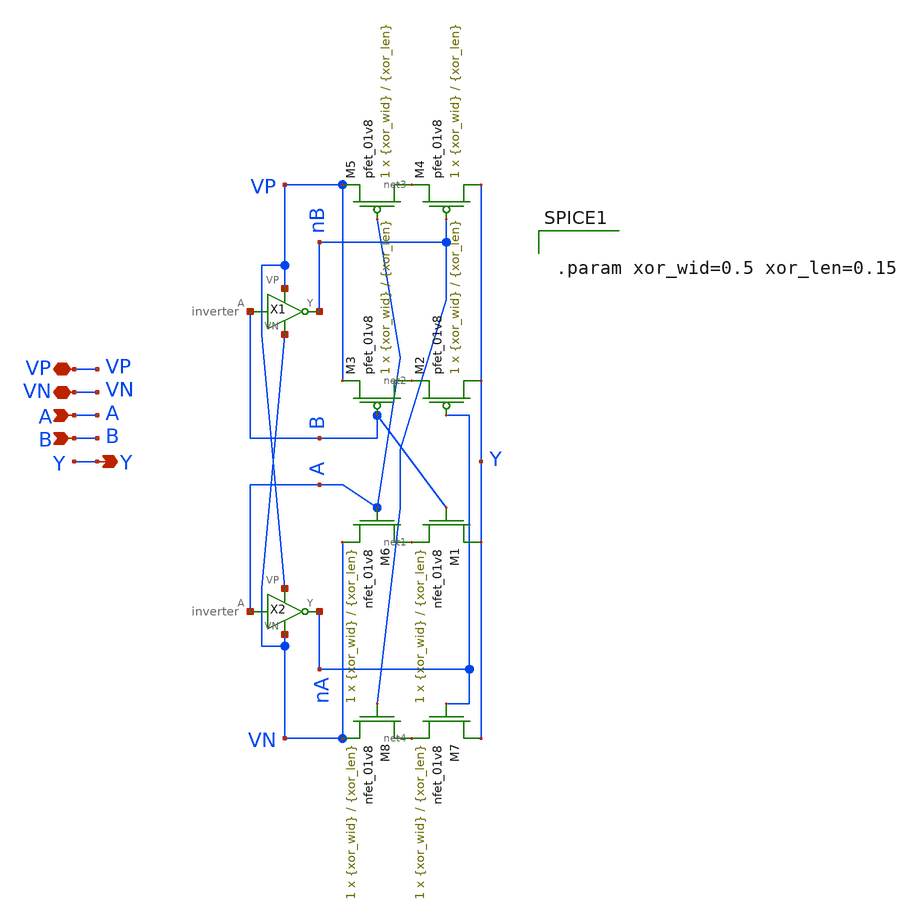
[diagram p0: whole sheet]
** sch_path: LDS/LDS_xor.sch
**.subckt LDS_xor VN VP Y A B
*.iopin VN
*.iopin VP
*.opin Y
*.ipin A
*.ipin B
X2 A nA VP VN inverter
X1 B nB VP VN inverter
XM1 Y B net1 VN sky130_fd_pr__nfet_01v8 L={xor_len} W={xor_wid} nf=1 ad='int((nf+1)/2) * W/nf * 0.29'
+ as='int((nf+2)/2) * W/nf * 0.29' pd='2*int((nf+1)/2) * (W/nf + 0.29)' ps='2*int((nf+2)/2) * (W/nf + 0.29)'
+ nrd='0.29 / W' nrs='0.29 / W' sa=0 sb=0 sd=0 mult=1 m=1
XM2 Y nA net2 VP sky130_fd_pr__pfet_01v8 L={xor_len} W={xor_wid} nf=1 ad='int((nf+1)/2) * W/nf * 0.29'
+ as='int((nf+2)/2) * W/nf * 0.29' pd='2*int((nf+1)/2) * (W/nf + 0.29)' ps='2*int((nf+2)/2) * (W/nf + 0.29)'
+ nrd='0.29 / W' nrs='0.29 / W' sa=0 sb=0 sd=0 mult=1 m=1
XM3 net2 B VP VP sky130_fd_pr__pfet_01v8 L={xor_len} W={xor_wid} nf=1 ad='int((nf+1)/2) * W/nf * 0.29'
+ as='int((nf+2)/2) * W/nf * 0.29' pd='2*int((nf+1)/2) * (W/nf + 0.29)' ps='2*int((nf+2)/2) * (W/nf + 0.29)'
+ nrd='0.29 / W' nrs='0.29 / W' sa=0 sb=0 sd=0 mult=1 m=1
XM4 Y nB net3 VP sky130_fd_pr__pfet_01v8 L={xor_len} W={xor_wid} nf=1 ad='int((nf+1)/2) * W/nf * 0.29'
+ as='int((nf+2)/2) * W/nf * 0.29' pd='2*int((nf+1)/2) * (W/nf + 0.29)' ps='2*int((nf+2)/2) * (W/nf + 0.29)'
+ nrd='0.29 / W' nrs='0.29 / W' sa=0 sb=0 sd=0 mult=1 m=1
XM5 net3 A VP VP sky130_fd_pr__pfet_01v8 L={xor_len} W={xor_wid} nf=1 ad='int((nf+1)/2) * W/nf * 0.29'
+ as='int((nf+2)/2) * W/nf * 0.29' pd='2*int((nf+1)/2) * (W/nf + 0.29)' ps='2*int((nf+2)/2) * (W/nf + 0.29)'
+ nrd='0.29 / W' nrs='0.29 / W' sa=0 sb=0 sd=0 mult=1 m=1
XM6 net1 A VN VN sky130_fd_pr__nfet_01v8 L={xor_len} W={xor_wid} nf=1 ad='int((nf+1)/2) * W/nf * 0.29'
+ as='int((nf+2)/2) * W/nf * 0.29' pd='2*int((nf+1)/2) * (W/nf + 0.29)' ps='2*int((nf+2)/2) * (W/nf + 0.29)'
+ nrd='0.29 / W' nrs='0.29 / W' sa=0 sb=0 sd=0 mult=1 m=1
XM7 Y nA net4 VN sky130_fd_pr__nfet_01v8 L={xor_len} W={xor_wid} nf=1 ad='int((nf+1)/2) * W/nf * 0.29'
+ as='int((nf+2)/2) * W/nf * 0.29' pd='2*int((nf+1)/2) * (W/nf + 0.29)' ps='2*int((nf+2)/2) * (W/nf + 0.29)'
+ nrd='0.29 / W' nrs='0.29 / W' sa=0 sb=0 sd=0 mult=1 m=1
XM8 net4 nB VN VN sky130_fd_pr__nfet_01v8 L={xor_len} W={xor_wid} nf=1 ad='int((nf+1)/2) * W/nf * 0.29'
+ as='int((nf+2)/2) * W/nf * 0.29' pd='2*int((nf+1)/2) * (W/nf + 0.29)' ps='2*int((nf+2)/2) * (W/nf + 0.29)'
+ nrd='0.29 / W' nrs='0.29 / W' sa=0 sb=0 sd=0 mult=1 m=1
**** begin user architecture code


.param xor_wid=0.5 xor_len=0.15


**** end user architecture code
**.ends

* expanding   symbol:  inverter.sym # of pins=4
** sym_path: LDS/inverter.sym
** sch_path: LDS/inverter.sch
.subckt inverter A Y VP VN
*.iopin VP
*.ipin A
*.opin Y
*.iopin VN
XM2 Y A VP VP sky130_fd_pr__pfet_01v8 L={inv_len} W={inv_wid} nf=1 ad='int((nf+1)/2) * W/nf * 0.29' as='int((nf+2)/2) * W/nf * 0.29'
+ pd='2*int((nf+1)/2) * (W/nf + 0.29)' ps='2*int((nf+2)/2) * (W/nf + 0.29)' nrd='0.29 / W' nrs='0.29 / W'
+ sa=0 sb=0 sd=0 mult=1 m=1
XM1 Y A VN VN sky130_fd_pr__nfet_01v8 L={inv_len} W={inv_wid} nf=1 ad='int((nf+1)/2) * W/nf * 0.29' as='int((nf+2)/2) * W/nf * 0.29'
+ pd='2*int((nf+1)/2) * (W/nf + 0.29)' ps='2*int((nf+2)/2) * (W/nf + 0.29)' nrd='0.29 / W' nrs='0.29 / W'
+ sa=0 sb=0 sd=0 mult=1 m=1
.ends

.end
